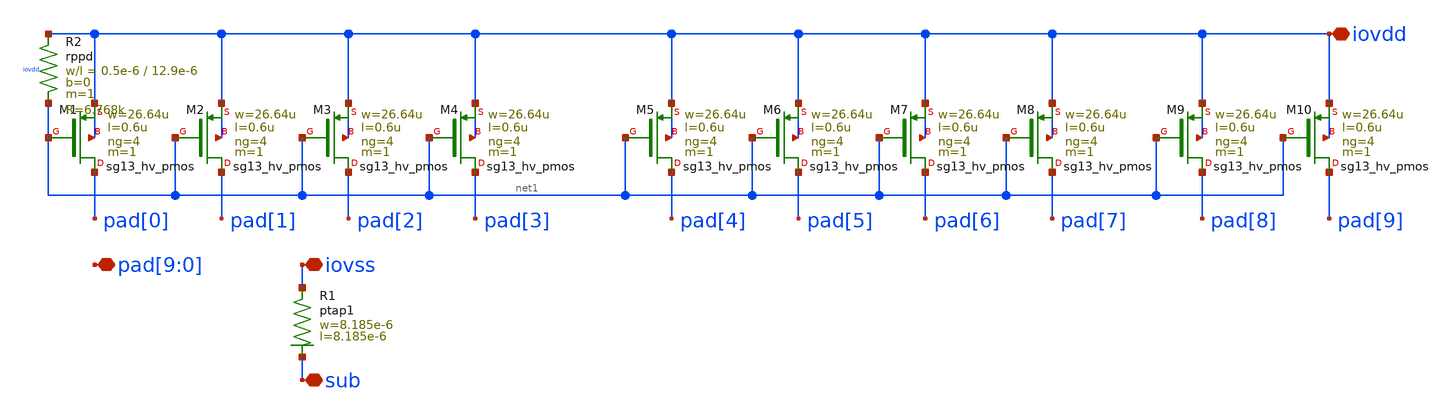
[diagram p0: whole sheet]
** sch_path: ihp-sg13g2/sg13g2_io/xschem/sg13g2_Clamp_P20N0D.sch
**.subckt sg13g2_Clamp_P20N0D iovss iovdd
*+ pad[9],pad[8],pad[7],pad[6],pad[5],pad[4],pad[3],pad[2],pad[1],pad[0] sub
*.iopin iovss
*.iopin iovdd
*.iopin pad[9],pad[8],pad[7],pad[6],pad[5],pad[4],pad[3],pad[2],pad[1],pad[0]
*.iopin sub
XR1 iovss sub ptap1 R=9.826 w=8.185e-6 l=8.185e-6
XM1 pad[0] net1 iovdd iovdd sg13_hv_pmos w=26.64u l=0.6u ng=4 m=1 mm_ok=1
XM2 pad[1] net1 iovdd iovdd sg13_hv_pmos w=26.64u l=0.6u ng=4 m=1 mm_ok=1
XM3 pad[2] net1 iovdd iovdd sg13_hv_pmos w=26.64u l=0.6u ng=4 m=1 mm_ok=1
XM4 pad[3] net1 iovdd iovdd sg13_hv_pmos w=26.64u l=0.6u ng=4 m=1 mm_ok=1
XM5 pad[4] net1 iovdd iovdd sg13_hv_pmos w=26.64u l=0.6u ng=4 m=1 mm_ok=1
XM6 pad[5] net1 iovdd iovdd sg13_hv_pmos w=26.64u l=0.6u ng=4 m=1 mm_ok=1
XM7 pad[6] net1 iovdd iovdd sg13_hv_pmos w=26.64u l=0.6u ng=4 m=1 mm_ok=1
XM8 pad[7] net1 iovdd iovdd sg13_hv_pmos w=26.64u l=0.6u ng=4 m=1 mm_ok=1
XM9 pad[8] net1 iovdd iovdd sg13_hv_pmos w=26.64u l=0.6u ng=4 m=1 mm_ok=1
XM10 pad[9] net1 iovdd iovdd sg13_hv_pmos w=26.64u l=0.6u ng=4 m=1 mm_ok=1
XR2 iovdd net1 iovdd rppd w=0.5e-6 l=12.9e-6 m=1 b=0 mm_ok=1
**.ends
.end
